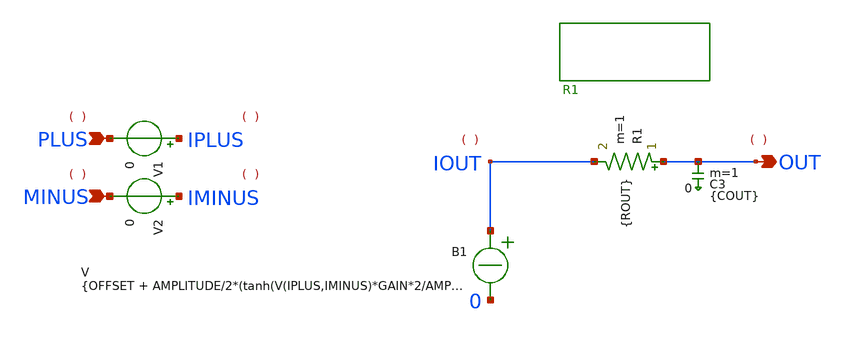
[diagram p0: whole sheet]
** sch_path: xschem_library_oa/ngspice/comp_ngspice/schematic/comp_ngspice.sch
* Copyright (C) 1998-2024 Stefan Frederik Schippers
* This program is free software; you can redistribute it and/or modify
* it under the terms of the GNU General Public License as published by
* the Free Software Foundation; either version 2 of the License, or
* (at your option) any later version.
* This program is distributed in the hope that it will be useful,
* but WITHOUT ANY WARRANTY; without even the implied warranty of
* MERCHANTABILITY or FITNESS FOR A PARTICULAR PURPOSE.  See the
* GNU General Public License for more details.
* You should have received a copy of the GNU General Public License
* along with this program; if not, write to the Free Software
**.subckt comp_ngspice PLUS MINUS OUT
*.ipin PLUS
*.ipin MINUS
*.opin OUT
B1 IOUT 0 V = {OFFSET + AMPLITUDE/2*(tanh(V(IPLUS,IMINUS)*GAIN*2/AMPLITUDE))}
R1 OUT IOUT {ROUT} m=1
C3 OUT 0 {COUT} m=1
V1 IPLUS PLUS 0
V2 IMINUS MINUS 0
**.ends
.end
